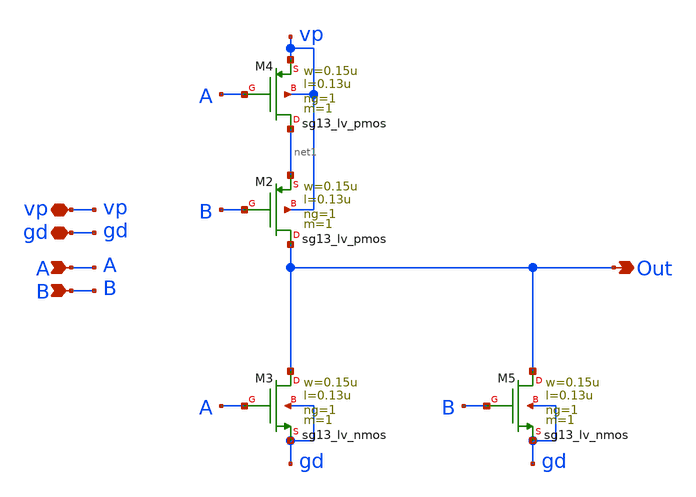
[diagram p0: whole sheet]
** sch_path: schematics/divider/schematics/NOR_2in_dek.sch
**.subckt NOR_2in_dek Out gd A vp B
*.opin Out
*.iopin gd
*.ipin A
*.iopin vp
*.ipin B
XM3 Out A gd gd sg13_lv_nmos w=0.15u l=0.13u ng=1 m=1 mm_ok=1
XM2 Out B net1 vp sg13_lv_pmos w=0.15u l=0.13u ng=1 m=1 mm_ok=1
XM4 net1 A vp vp sg13_lv_pmos w=0.15u l=0.13u ng=1 m=1 mm_ok=1
XM5 Out B gd gd sg13_lv_nmos w=0.15u l=0.13u ng=1 m=1 mm_ok=1
**.ends
.end
